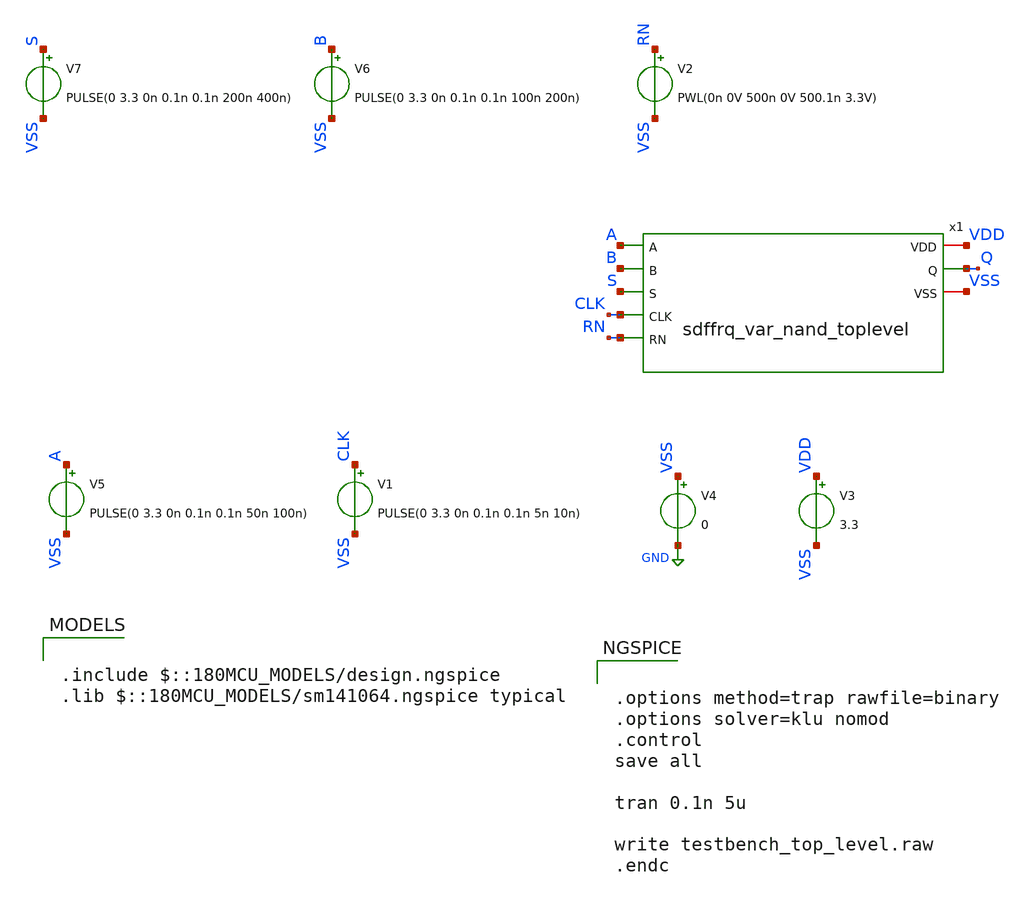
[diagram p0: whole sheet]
** sch_path: designs/libs/tb_toplevel/testbench_sdffrq_mux_nand.sch
**.subckt testbench_sdffrq_mux_nand
V1 CLK VSS PULSE(0 3.3 0n 0.1n 0.1n 5n 10n)
V3 VDD VSS 3.3
V4 VSS GND 0
V5 A VSS PULSE(0 3.3 0n 0.1n 0.1n 50n 100n)
V6 B VSS PULSE(0 3.3 0n 0.1n 0.1n 100n 200n)
V7 S VSS PULSE(0 3.3 0n 0.1n 0.1n 200n 400n)
V2 RN VSS PWL(0n 0V 500n 0V 500.1n 3.3V)
x1 VDD A Q B S CLK RN VSS sdffrq_var_nand_toplevel
**** begin user architecture code

.include $::180MCU_MODELS/design.ngspice
.lib $::180MCU_MODELS/sm141064.ngspice typical



.options method=trap rawfile=binary
.options solver=klu nomod
.control
save all

tran 0.1n 5u

write testbench_top_level.raw
.endc


**** end user architecture code
**.ends
.GLOBAL GND
.end
